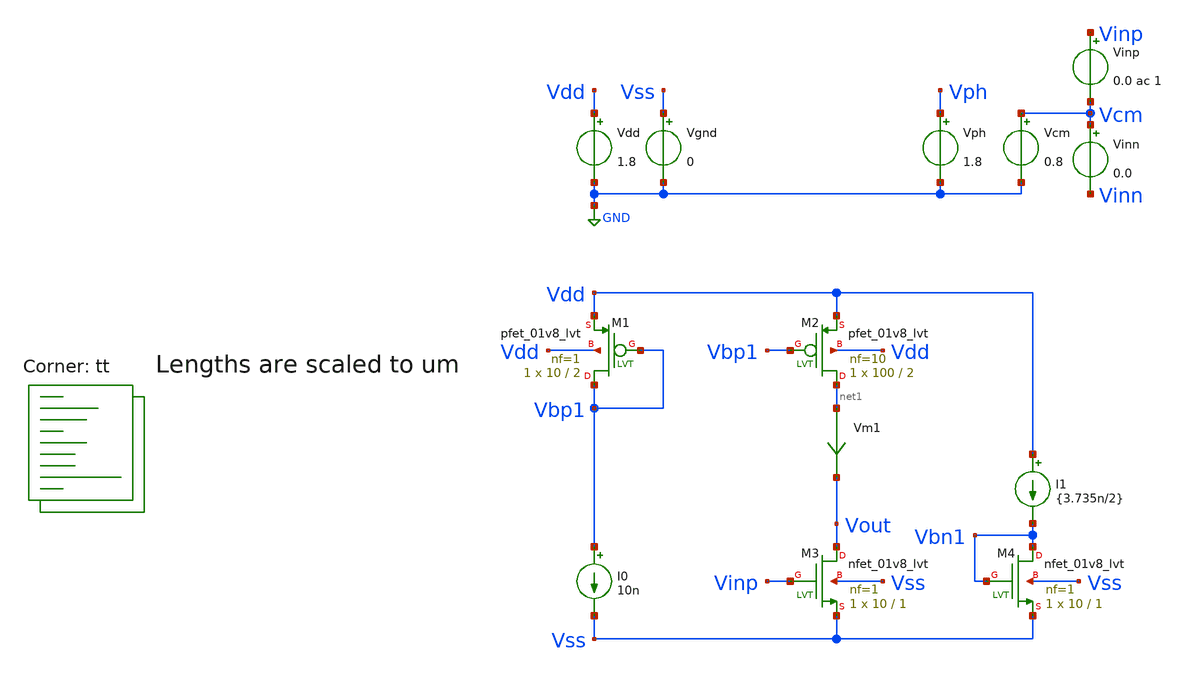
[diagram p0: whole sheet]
** sch_path: ic/CntDiffAmp/Testbench/AuxSim.sch
**.subckt AuxSim
I0 Vbp1 Vss 10n
Vdd Vdd GND 1.8
Vgnd Vss GND 0
Vinp Vinp Vcm 0.0 ac 1
Vinn Vcm Vinn 0.0
Vph Vph GND 1.8
Vcm Vcm GND 0.8
XM1 Vbp1 Vbp1 Vdd Vdd sky130_fd_pr__pfet_01v8_lvt L=2 W=10 nf=1 ad='int((nf+1)/2) * W/nf * 0.29' as='int((nf+2)/2) * W/nf * 0.29'
+ pd='2*int((nf+1)/2) * (W/nf + 0.29)' ps='2*int((nf+2)/2) * (W/nf + 0.29)' nrd='0.29 / W' nrs='0.29 / W'
+ sa=0 sb=0 sd=0 mult=1 m=1
XM2 net1 Vbp1 Vdd Vdd sky130_fd_pr__pfet_01v8_lvt L=2 W=100 nf=10 ad='int((nf+1)/2) * W/nf * 0.29' as='int((nf+2)/2) * W/nf * 0.29'
+ pd='2*int((nf+1)/2) * (W/nf + 0.29)' ps='2*int((nf+2)/2) * (W/nf + 0.29)' nrd='0.29 / W' nrs='0.29 / W'
+ sa=0 sb=0 sd=0 mult=1 m=1
XM3 Vout Vinp Vss Vss sky130_fd_pr__nfet_01v8_lvt L=1 W=10 nf=1 ad='int((nf+1)/2) * W/nf * 0.29' as='int((nf+2)/2) * W/nf * 0.29'
+ pd='2*int((nf+1)/2) * (W/nf + 0.29)' ps='2*int((nf+2)/2) * (W/nf + 0.29)' nrd='0.29 / W' nrs='0.29 / W'
+ sa=0 sb=0 sd=0 mult=1 m=1
Vm1 net1 Vout 0
.save i(vm1)
XM4 Vbn1 Vbn1 Vss Vss sky130_fd_pr__nfet_01v8_lvt L=1 W=10 nf=1 ad='int((nf+1)/2) * W/nf * 0.29' as='int((nf+2)/2) * W/nf * 0.29'
+ pd='2*int((nf+1)/2) * (W/nf + 0.29)' ps='2*int((nf+2)/2) * (W/nf + 0.29)' nrd='0.29 / W' nrs='0.29 / W'
+ sa=0 sb=0 sd=0 mult=1 m=1
I1 Vdd Vbn1 {3.735n/2}
**** begin user architecture code
.lib $::SKYWATER_MODELS/sky130.lib.spice tt

* this option enables mos model bin
* selection based on W/NF instead of W
.option wnflag=1
.option savecurrents acct abstol=1e-15
*reltol=1e-6
*gmin=1e-15

.control
save all
save @m.xm1.msky130_fd_pr__pfet_01v8_lvt[gm]
save @m.xm1.msky130_fd_pr__pfet_01v8_lvt[vth]
save @m.xm1.msky130_fd_pr__pfet_01v8_lvt[vdsat]
save @m.xm2.msky130_fd_pr__pfet_01v8_lvt[gm]
save @m.xm2.msky130_fd_pr__pfet_01v8_lvt[vth]
save @m.xm2.msky130_fd_pr__pfet_01v8_lvt[vdsat]
save @m.xm3.msky130_fd_pr__nfet_01v8_lvt[gm]
save @m.xm3.msky130_fd_pr__nfet_01v8_lvt[vth]
save @m.xm3.msky130_fd_pr__nfet_01v8_lvt[vdsat]

op
write AuxSim.raw

dc Vcm 0.0 1.8 0.01
plot v(Vout), v(Vbp1) vs v(Vcm)
plot i(Vm1) vs v(Vcm)
plot @m.xm2.msky130_fd_pr__pfet_01v8_lvt[gm], @m.xm3.msky130_fd_pr__nfet_01v8_lvt[gm] vs V(Vcm)

set appendwrite
write AuxSim.raw

ac dec 10 1 1e9
plot db(v(Vout))

write AuxSim.raw
.endc




** CntFET model
.subckt cntnfet_a d g s b
.param l=1 w=0.01 mult=1
mcntnfet_a d g s b cntnfet l={l} w={w}
* BSIM4 model
.model cntnfet nmos  level=54 version=4.8.2  toxe=7e-9
.ends cntnfet_a

.subckt cntpfet_a d g s b
.param l=1 w=0.01 mult=1
mcntpfet_a d g s b cntpfet l={l} w={w}
* BSIM4 model
.model cntpfet pmos  level=54 version=4.8.2  toxe=100e-9 U0=1.09e-4 VTH0=-2.02
.ends cntnfet_a

.model cntnfet_b nmos level=54 version=4.8.2 toxe=5e-9
.model cntpfet_b nmos level=54 version=4.8.2 toxe=5e-9


**** end user architecture code
**.ends
.GLOBAL GND
.end
